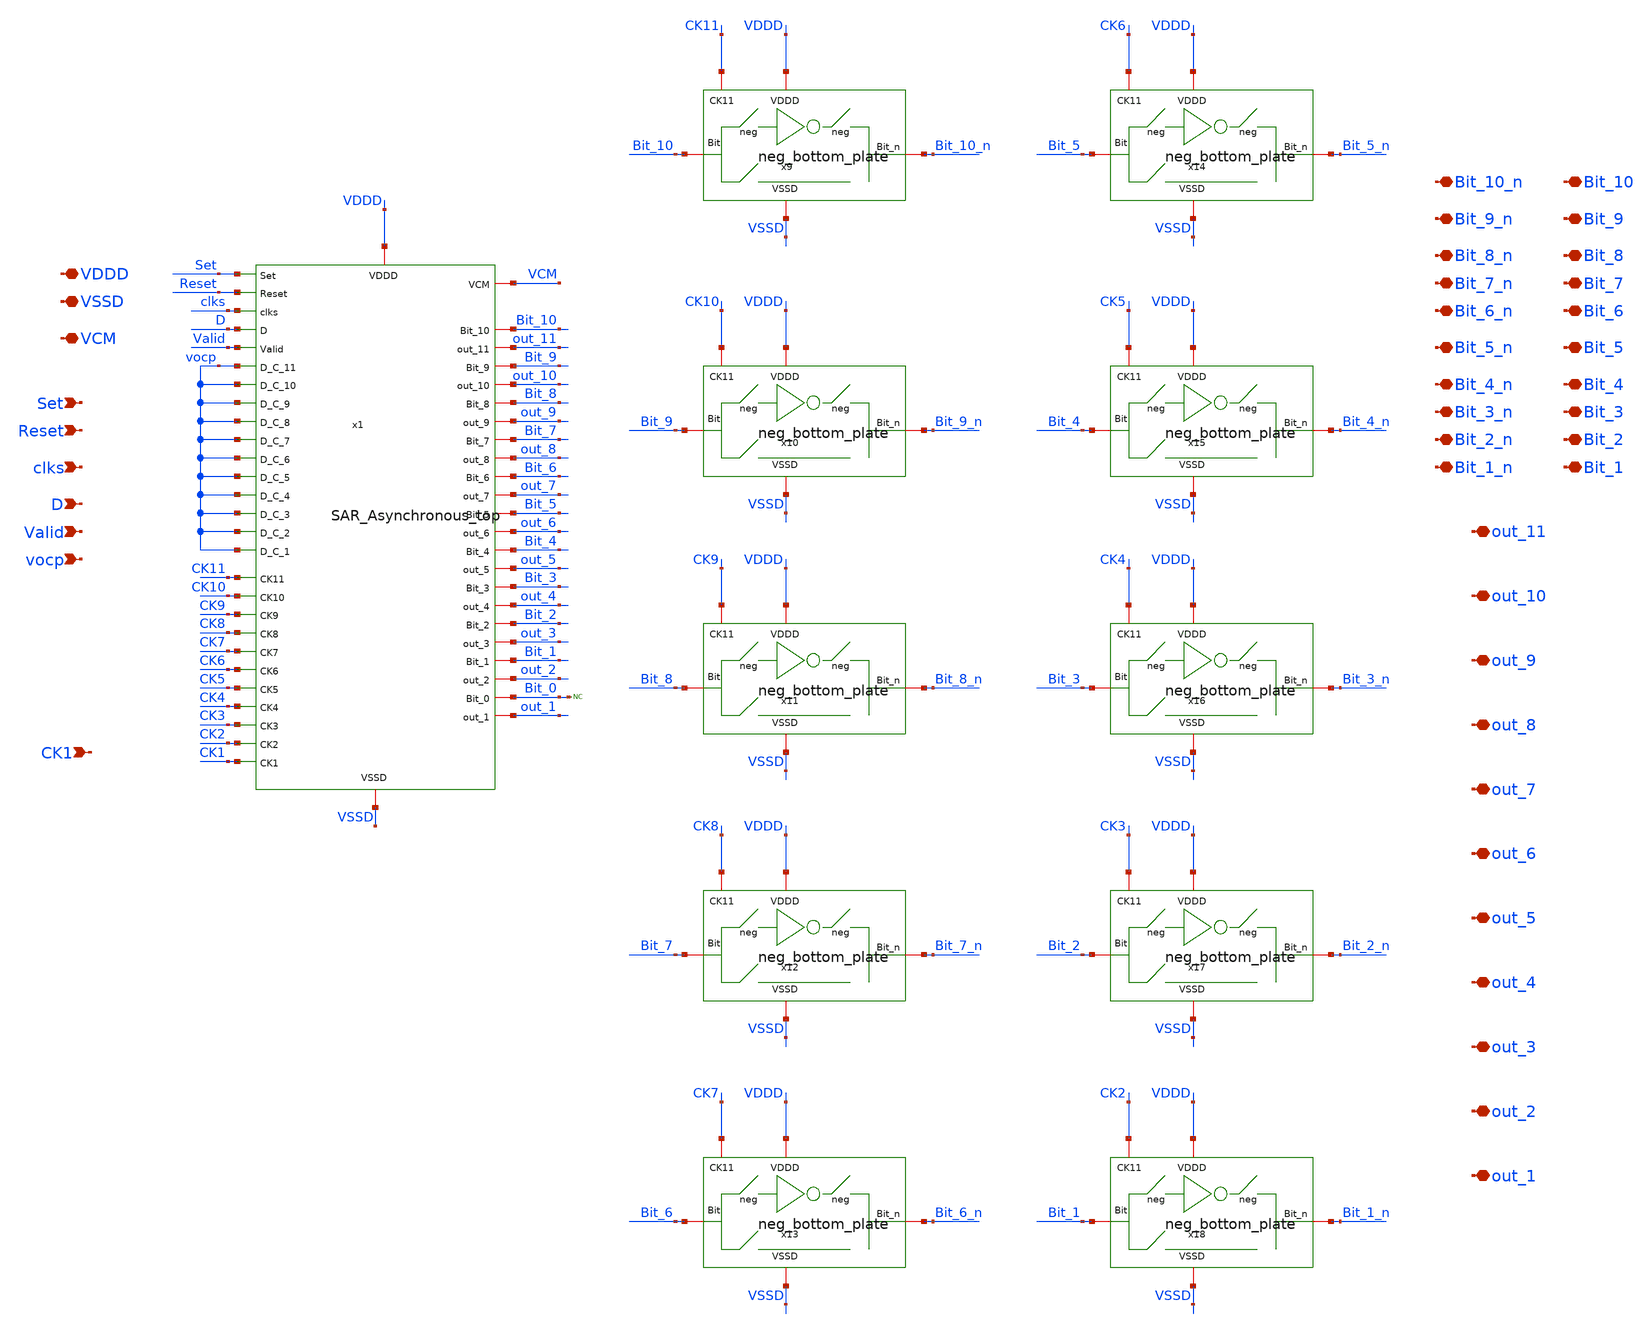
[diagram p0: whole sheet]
** sch_path: SAR_ADC/SAR_Asynchronous_top_neg_logic/SAR_Asynchronous_top_neg_logic.sch
**.subckt SAR_Asynchronous_top_neg_logic VDDD VSSD Set Reset VCM clks D Valid vocp Bit_10_n Bit_9_n
*+ Bit_8_n Bit_7_n Bit_6_n Bit_5_n Bit_4_n Bit_3_n Bit_2_n Bit_1_n out_11 out_10 out_9 out_8 out_7 out_6 out_5
*+ out_4 out_3 out_2 out_1 Bit_10 Bit_9 Bit_8 Bit_7 Bit_6 Bit_5 Bit_4 Bit_3 Bit_2 Bit_1 CK1
*.iopin VDDD
*.iopin VSSD
*.ipin Set
*.ipin Reset
*.iopin VCM
*.ipin clks
*.ipin D
*.ipin Valid
*.ipin vocp
*.iopin Bit_10_n
*.iopin Bit_9_n
*.iopin Bit_8_n
*.iopin Bit_7_n
*.iopin Bit_6_n
*.iopin Bit_5_n
*.iopin Bit_4_n
*.iopin Bit_3_n
*.iopin Bit_2_n
*.iopin Bit_1_n
*.iopin out_11
*.iopin out_10
*.iopin out_9
*.iopin out_8
*.iopin out_7
*.iopin out_6
*.iopin out_5
*.iopin out_4
*.iopin out_3
*.iopin out_2
*.iopin out_1
*.iopin Bit_10
*.iopin Bit_9
*.iopin Bit_8
*.iopin Bit_7
*.iopin Bit_6
*.iopin Bit_5
*.iopin Bit_4
*.iopin Bit_3
*.iopin Bit_2
*.iopin Bit_1
*.ipin CK1
x1 VDDD VSSD VCM Set Reset clks Bit_10 D out_11 Valid Bit_9 out_10 Bit_8 out_9 Bit_7 out_8 Bit_6
+ out_7 Bit_5 out_6 Bit_4 out_5 Bit_3 out_4 Bit_2 out_3 Bit_1 out_2 Bit_0 out_1 vocp vocp vocp vocp vocp
+ vocp vocp vocp vocp vocp vocp CK10 CK9 CK8 CK7 CK6 CK5 CK4 CK3 CK2 CK1 CK11 SAR_Asynchronous_top
x9 VDDD VSSD CK11 Bit_10 Bit_10_n neg_bottom_plate
x10 VDDD VSSD CK10 Bit_9 Bit_9_n neg_bottom_plate
x11 VDDD VSSD CK9 Bit_8 Bit_8_n neg_bottom_plate
x12 VDDD VSSD CK8 Bit_7 Bit_7_n neg_bottom_plate
x13 VDDD VSSD CK7 Bit_6 Bit_6_n neg_bottom_plate
x14 VDDD VSSD CK6 Bit_5 Bit_5_n neg_bottom_plate
x15 VDDD VSSD CK5 Bit_4 Bit_4_n neg_bottom_plate
x16 VDDD VSSD CK4 Bit_3 Bit_3_n neg_bottom_plate
x17 VDDD VSSD CK3 Bit_2 Bit_2_n neg_bottom_plate
x18 VDDD VSSD CK2 Bit_1 Bit_1_n neg_bottom_plate
* noconn Bit_0
**.ends
.end
